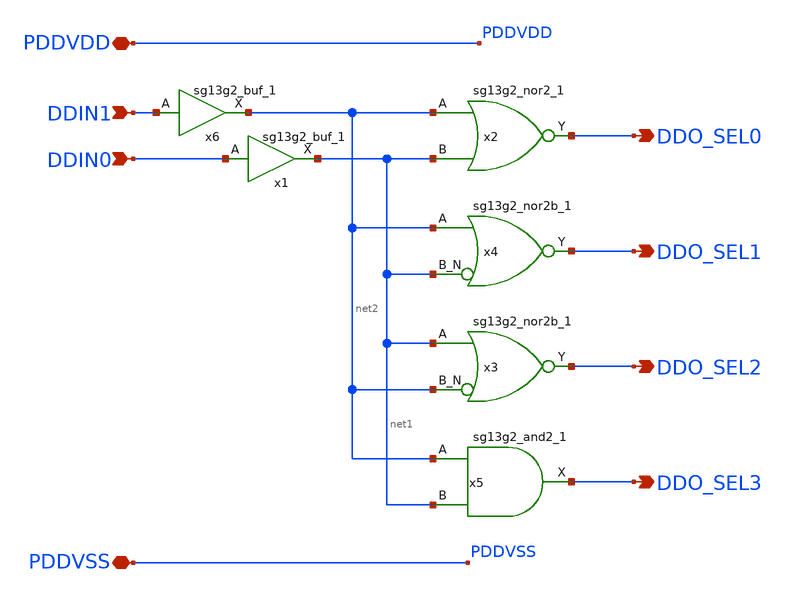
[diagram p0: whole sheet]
** sch_path: xschem/digital_decoder.bak.sch
* IHP-GmbH/IHP-Open-PDK/ihp-sg13g2/libs.tech/xschem/sg13g2_stdcells/sg13g2_buf_1.sch:
* Copyright 2023 IHP PDK Authors
* Licensed under the Apache License, Version 2.0 (the "License");
**.subckt digital_decoder.bak PDDVDD DDIN1 DDO_SEL0 PDDVSS DDIN0 DDO_SEL1 DDO_SEL2 DDO_SEL3
*.iopin PDDVDD
*.ipin DDIN1
*.opin DDO_SEL0
*.iopin PDDVSS
*.ipin DDIN0
*.opin DDO_SEL1
*.opin DDO_SEL2
*.opin DDO_SEL3
x3 DDO_SEL2 net1 net2 PDDVDD PDDVSS sg13g2_nor2b_1
x4 DDO_SEL1 net2 net1 PDDVDD PDDVSS sg13g2_nor2b_1
x5 DDO_SEL3 net2 net1 PDDVDD PDDVSS sg13g2_and2_1
x1 net1 DDIN0 PDDVDD PDDVSS sg13g2_buf_1
x6 net2 DDIN1 PDDVDD PDDVSS sg13g2_buf_1
x2 DDO_SEL0 net2 net1 VDD VSS sg13g2_nor2_1
**.ends

* expanding   symbol:  sg13g2_stdcells/sg13g2_nor2b_1.sym # of pins=3
** sym_path: sg13g2_stdcells/sg13g2_nor2b_1.sym
** sch_path: sg13g2_stdcells/sg13g2_nor2b_1.sch
.subckt sg13g2_nor2b_1 Y A B_N VDD VSS
*.opin Y
*.ipin B_N
*.ipin A
*.iopin VDD
*.iopin VSS
XM1 B B_N VSS VSS sg13_lv_nmos w=550.00n l=130.00n ng=1 m=1 mm_ok=1
XM2 Y A VSS VSS sg13_lv_nmos w=740.00n l=130.00n ng=1 m=1 mm_ok=1
XM3 Y B VSS VSS sg13_lv_nmos w=740.00n l=130.00n ng=1 m=1 mm_ok=1
XM4 B B_N VDD VDD sg13_lv_pmos w=840.00n l=130.00n ng=1 m=1 mm_ok=1
XM5 net1 B VDD VDD sg13_lv_pmos w=1.12u l=130.00n ng=1 m=1 mm_ok=1
XM6 Y A net1 VDD sg13_lv_pmos w=1.12u l=130.00n ng=1 m=1 mm_ok=1
.ends


* expanding   symbol:  sg13g2_stdcells/sg13g2_and2_1.sym # of pins=3
** sym_path: sg13g2_stdcells/sg13g2_and2_1.sym
** sch_path: sg13g2_stdcells/sg13g2_and2_1.sch
.subckt sg13g2_and2_1 X A B VDD VSS
*.ipin A
*.ipin B
*.opin X
*.iopin VDD
*.iopin VSS
XM1 net1 A net2 VSS sg13_lv_nmos w=640.00n l=130.00n ng=1 m=1 mm_ok=1
XM2 net2 B VSS VSS sg13_lv_nmos w=640.00n l=130.00n ng=1 m=1 mm_ok=1
XM3 X net1 VSS VSS sg13_lv_nmos w=740.00n l=130.00n ng=1 m=1 mm_ok=1
XM4 net1 B VDD VDD sg13_lv_pmos w=840.00n l=130.00n ng=1 m=1 mm_ok=1
XM5 net1 A VDD VDD sg13_lv_pmos w=840.00n l=130.00n ng=1 m=1 mm_ok=1
XM6 X net1 VDD VDD sg13_lv_pmos w=1.12u l=130.00n ng=1 m=1 mm_ok=1
.ends


* expanding   symbol:  sg13g2_stdcells/sg13g2_buf_1.sym # of pins=2
** sym_path: sg13g2_stdcells/sg13g2_buf_1.sym
** sch_path: sg13g2_stdcells/sg13g2_buf_1.sch
.subckt sg13g2_buf_1 X A VDD VSS
*.ipin A
*.opin X
*.iopin VDD
*.iopin VSS
XM1 net1 A VSS VSS sg13_lv_nmos w=550.00n l=130.00n ng=1 m=1 mm_ok=1
XM2 X net1 VSS VSS sg13_lv_nmos w=740.00n l=130.00n ng=1 m=1 mm_ok=1
XM3 net1 A VDD VDD sg13_lv_pmos w=840.00n l=130.00n ng=1 m=1 mm_ok=1
XM4 X net1 VDD VDD sg13_lv_pmos w=1.12u l=130.00n ng=1 m=1 mm_ok=1
.ends


* expanding   symbol:  sg13g2_stdcells/sg13g2_nor2_1.sym # of pins=3
** sym_path: sg13g2_stdcells/sg13g2_nor2_1.sym
** sch_path: sg13g2_stdcells/sg13g2_nor2_1.sch
.subckt sg13g2_nor2_1 Y A B VDD VSS
*.opin Y
*.ipin B
*.ipin A
*.iopin VDD
*.iopin VSS
XM1 Y A VSS VSS sg13_lv_nmos w=740.00n l=130.00n ng=1 m=1 mm_ok=1
XM2 Y B VSS VSS sg13_lv_nmos w=740.00n l=130.00n ng=1 m=1 mm_ok=1
XM3 net1 A VDD VDD sg13_lv_pmos w=1.12u l=130.00n ng=1 m=1 mm_ok=1
XM4 Y B net1 VDD sg13_lv_pmos w=1.12u l=130.00n ng=1 m=1 mm_ok=1
.ends

.end
